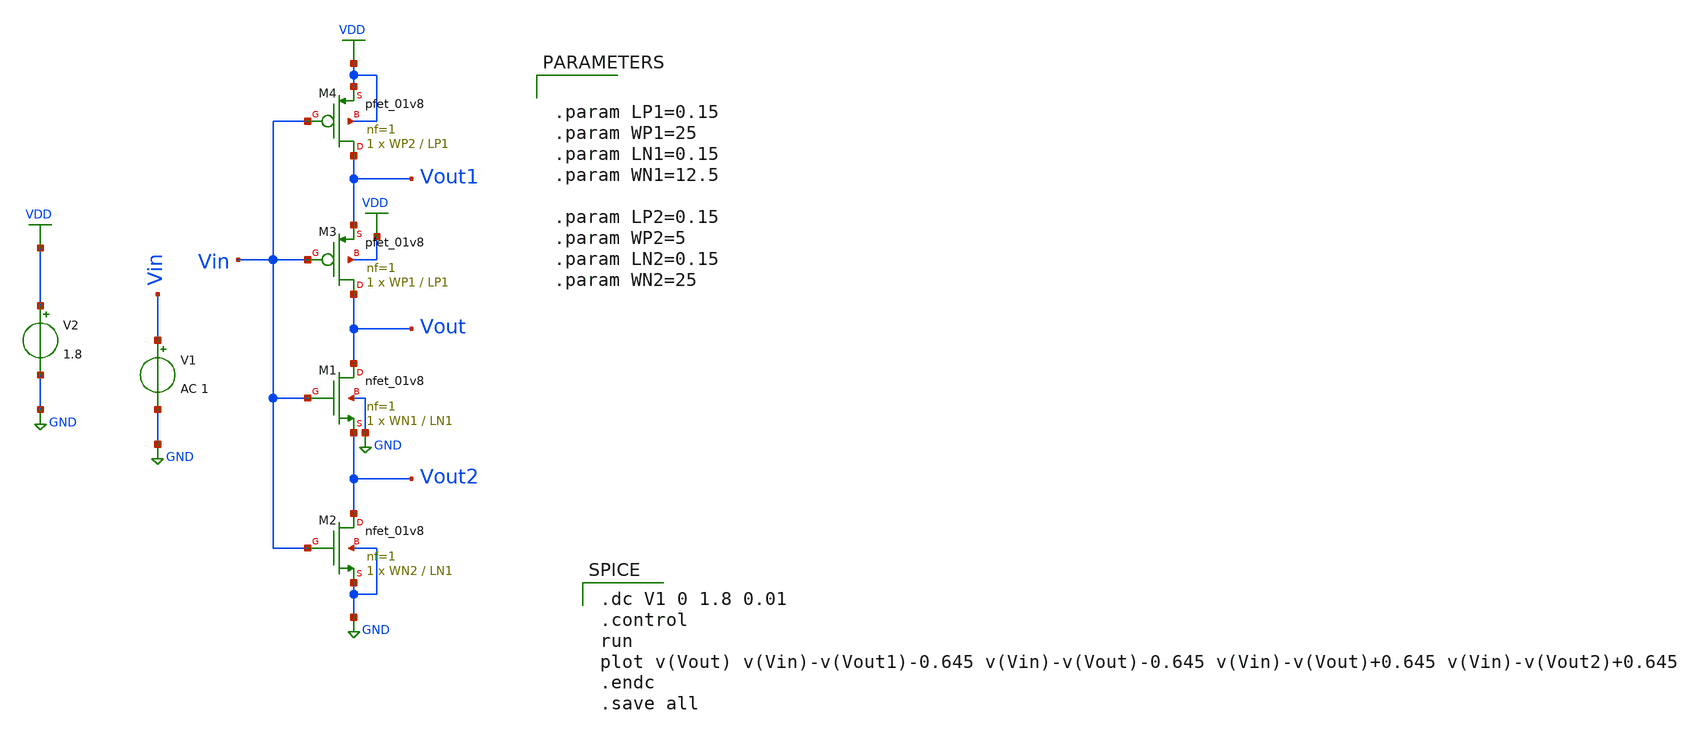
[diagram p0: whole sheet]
** sch_path: LIQAF circuit/test.sch
**.subckt test
XM1 Vout Vin Vout2 GND sky130_fd_pr__nfet_01v8 L=LN1 W=WN1 nf=1 ad='int((nf+1)/2) * W/nf * 0.29' as='int((nf+2)/2) * W/nf * 0.29'
+ pd='2*int((nf+1)/2) * (W/nf + 0.29)' ps='2*int((nf+2)/2) * (W/nf + 0.29)' nrd='0.29 / W' nrs='0.29 / W'
+ sa=0 sb=0 sd=0 mult=1 m=1
V1 Vin GND AC 1
V2 VDD GND 1.8
XM2 Vout2 Vin GND GND sky130_fd_pr__nfet_01v8 L=LN1 W=WN2 nf=1 ad='int((nf+1)/2) * W/nf * 0.29' as='int((nf+2)/2) * W/nf * 0.29'
+ pd='2*int((nf+1)/2) * (W/nf + 0.29)' ps='2*int((nf+2)/2) * (W/nf + 0.29)' nrd='0.29 / W' nrs='0.29 / W'
+ sa=0 sb=0 sd=0 mult=1 m=1
XM3 Vout Vin Vout1 VDD sky130_fd_pr__pfet_01v8 L=LP1 W=WP1 nf=1 ad='int((nf+1)/2) * W/nf * 0.29' as='int((nf+2)/2) * W/nf * 0.29'
+ pd='2*int((nf+1)/2) * (W/nf + 0.29)' ps='2*int((nf+2)/2) * (W/nf + 0.29)' nrd='0.29 / W' nrs='0.29 / W'
+ sa=0 sb=0 sd=0 mult=1 m=1
XM4 Vout1 Vin VDD VDD sky130_fd_pr__pfet_01v8 L=LP1 W=WP2 nf=1 ad='int((nf+1)/2) * W/nf * 0.29' as='int((nf+2)/2) * W/nf * 0.29'
+ pd='2*int((nf+1)/2) * (W/nf + 0.29)' ps='2*int((nf+2)/2) * (W/nf + 0.29)' nrd='0.29 / W' nrs='0.29 / W'
+ sa=0 sb=0 sd=0 mult=1 m=1
**** begin user architecture code
 ** manual skywater pdks install (with patches applied)
* .lib $::SKYWATER_MODELS/models/sky130.lib.spice tt

** opencircuitdesign pdks install
.lib $::SKYWATER_MODELS/sky130.lib.spice tt

.param mc_mm_switch=0
.param mc_pr_switch=0
.param LP1=0.15


.dc V1 0 1.8 0.01
.control
run
plot v(Vout) v(Vin)-v(Vout1)-0.645 v(Vin)-v(Vout)-0.645 v(Vin)-v(Vout)+0.645 v(Vin)-v(Vout2)+0.645
.endc
.save all



.param LP1=0.15
.param WP1=25
.param LN1=0.15
.param WN1=12.5

.param LP2=0.15
.param WP2=5
.param LN2=0.15
.param WN2=25


**** end user architecture code
**.ends
.GLOBAL GND
.GLOBAL VDD
.end
